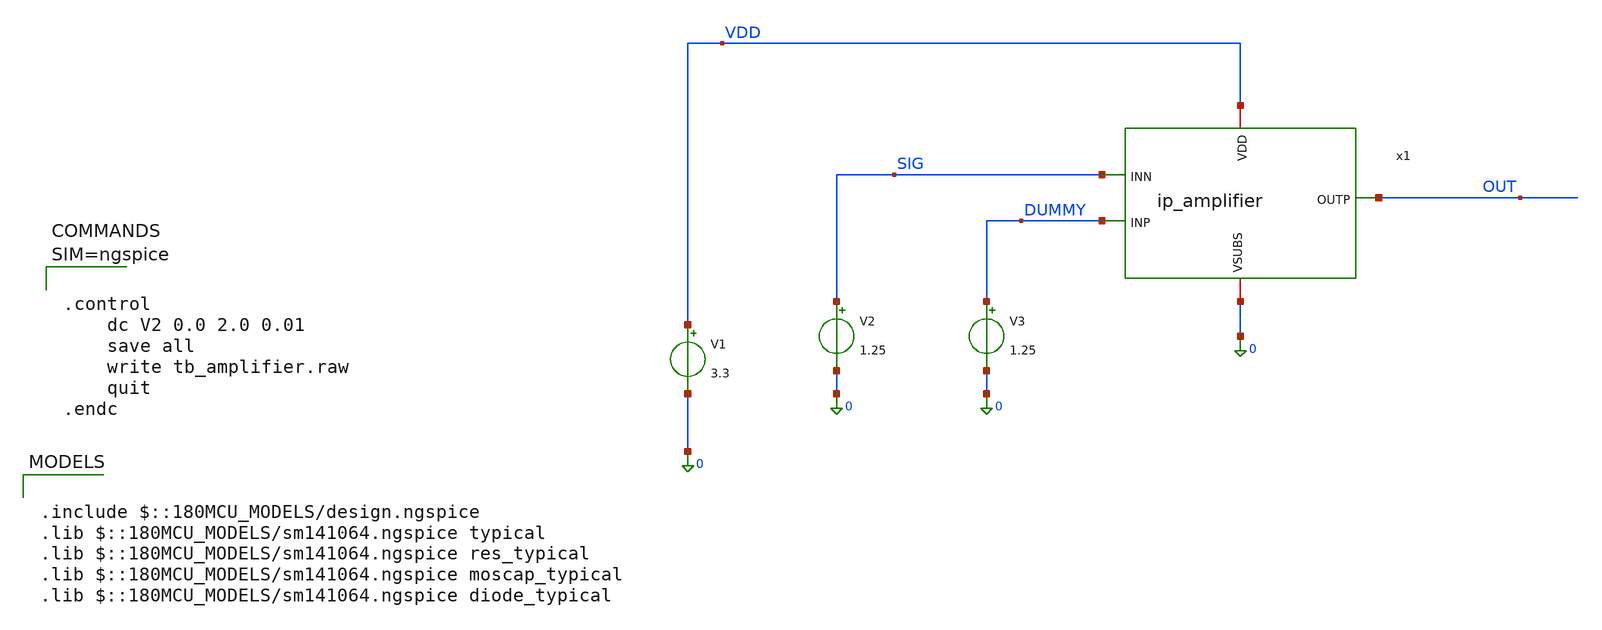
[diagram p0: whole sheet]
** sch_path: xschem/tb_amplifier.sch
**.subckt tb_amplifier
V1 VDD 0 3.3
x1 VDD OUT DUMMY SIG 0 ip_amplifier
V3 DUMMY 0 1.25
V2 SIG 0 1.25
**** begin user architecture code

.include $::180MCU_MODELS/design.ngspice
.lib $::180MCU_MODELS/sm141064.ngspice typical
.lib $::180MCU_MODELS/sm141064.ngspice res_typical
.lib $::180MCU_MODELS/sm141064.ngspice moscap_typical
.lib $::180MCU_MODELS/sm141064.ngspice diode_typical




.control
	dc V2 0.0 2.0 0.01
	save all
	write tb_amplifier.raw
	quit
.endc



**** end user architecture code
**.ends

* expanding   symbol:  ip_amplifier.sym # of pins=5
** sym_path: xschem/ip_amplifier.sym
** sch_path: xschem/ip_amplifier.sch
.subckt ip_amplifier VDD OUTP INP INN VSUBS
*.iopin VDD
*.iopin VSUBS
*.ipin INP
*.ipin INN
*.opin OUTP
XM1 OUTN INP net1 VDD pfet_03v3 L=0.5u W=15.0u nf=1 ad='int((nf+1)/2) * W/nf * 0.18u' as='int((nf+2)/2) * W/nf * 0.18u'
+ pd='2*int((nf+1)/2) * (W/nf + 0.18u)' ps='2*int((nf+2)/2) * (W/nf + 0.18u)' nrd='0.18u / W' nrs='0.18u / W'
+ sa=0 sb=0 sd=0 m=5 par=5
XM2 OUTP INN net2 VDD pfet_03v3 L=0.5u W=15.0u nf=1 ad='int((nf+1)/2) * W/nf * 0.18u' as='int((nf+2)/2) * W/nf * 0.18u'
+ pd='2*int((nf+1)/2) * (W/nf + 0.18u)' ps='2*int((nf+2)/2) * (W/nf + 0.18u)' nrd='0.18u / W' nrs='0.18u / W'
+ sa=0 sb=0 sd=0 m=5 par=5
R2 VSUBS OUTN 36k m=1
R3 VSUBS OUTP 36k m=1
I1 VDD net3 50u
R4 net2 net3 4.5k m=1
R1 net1 net3 400 m=1
.ends

.end
